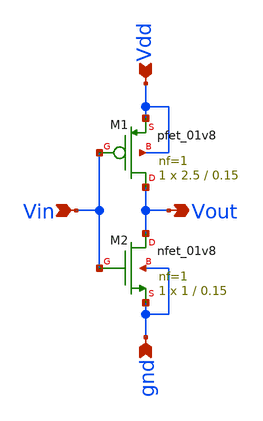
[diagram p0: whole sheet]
** sch_path: Design-and-analysis-of-CMOS-ineverter/XSCHEM FILES/CMOS.sch
**.subckt CMOS Vin Vdd gnd Vout
*.ipin Vin
*.ipin Vdd
*.ipin gnd
*.opin Vout
XM1 Vout Vin Vdd Vdd sky130_fd_pr__pfet_01v8 L=0.15 W=2.5 nf=1 ad='int((nf+1)/2) * W/nf * 0.29' as='int((nf+2)/2) * W/nf * 0.29'
+ pd='2*int((nf+1)/2) * (W/nf + 0.29)' ps='2*int((nf+2)/2) * (W/nf + 0.29)' nrd='0.29 / W' nrs='0.29 / W'
+ sa=0 sb=0 sd=0 mult=1 m=1
XM2 Vout Vin gnd gnd sky130_fd_pr__nfet_01v8 L=0.15 W=1 nf=1 ad='int((nf+1)/2) * W/nf * 0.29' as='int((nf+2)/2) * W/nf * 0.29'
+ pd='2*int((nf+1)/2) * (W/nf + 0.29)' ps='2*int((nf+2)/2) * (W/nf + 0.29)' nrd='0.29 / W' nrs='0.29 / W'
+ sa=0 sb=0 sd=0 mult=1 m=1
**.ends
.end
